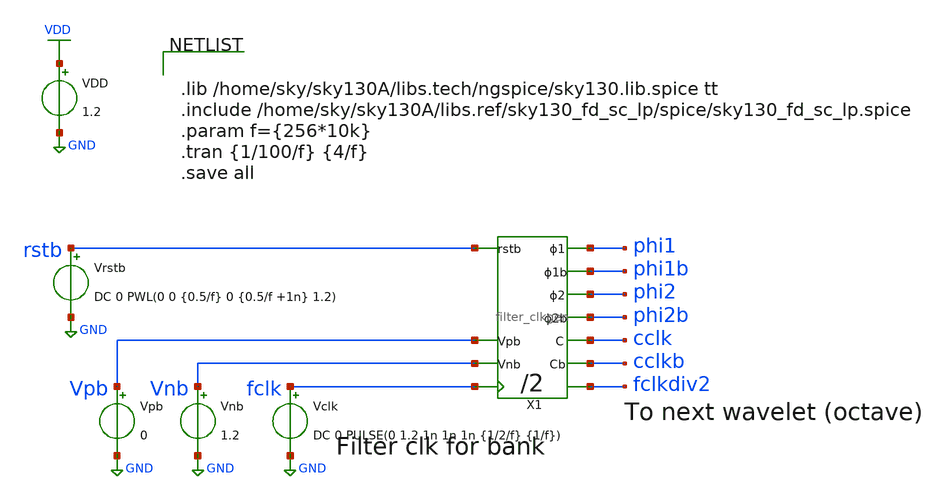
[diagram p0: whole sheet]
** sch_path: xschem/clkgen/filter_clkgen_tb.sch
**.subckt filter_clkgen_tb
Vrstb rstb GND DC 0 PWL(0 0 {0.5/f} 0 {0.5/f +1n} 1.2)
VDD VDD GND 1.2
Vpb Vpb GND 0
Vnb Vnb GND 1.2
Vclk fclk GND DC 0 PULSE(0 1.2 1n 1n 1n {1/2/f} {1/f})
X1 rstb fclk phi2b phi2 phi1b phi1 cclkb cclk fclkdiv2 Vpb Vnb filter_clkgen
**** begin user architecture code


.lib /home/sky/sky130A/libs.tech/ngspice/sky130.lib.spice tt
.include /home/sky/sky130A/libs.ref/sky130_fd_sc_lp/spice/sky130_fd_sc_lp.spice
.param f={256*10k}
.tran {1/100/f} {4/f}
.save all


**** end user architecture code
**.ends

* expanding   symbol:  clkgen/filter_clkgen.sym # of pins=11
** sym_path: xschem/clkgen/filter_clkgen.sym
** sch_path: xschem/clkgen/filter_clkgen.sch
.subckt filter_clkgen rstb clk phi2b phi2 phi1b phi1 cclkb cclk clkdiv2 Vpb Vnb
*.ipin clk
*.ipin rstb
*.opin phi2
*.opin phi2b
*.opin phi1
*.opin phi1b
*.opin cclk
*.opin cclkb
*.opin clkdiv2
*.ipin Vpb
*.ipin Vnb
x11 clk net3 rstb gnd gnd vdd vdd clkdiv2 net3 sky130_fd_sc_lp__dfrbp_1
X4 phi2dd phi2 phi2b comp_clks Wpmos=1.26 Lpmos=0.18 Wnmos=0.42 Lnmos=0.18
X7 phi1dd phi1 phi1b comp_clks Wpmos=1.26 Lpmos=0.18 Wnmos=0.42 Lnmos=0.18
X10 div2dd cclk cclkb comp_clks Wpmos=1.26 Lpmos=0.18 Wnmos=0.42 Lnmos=0.18
x12 clk rstb gnd gnd vdd vdd gclk sky130_fd_sc_lp__dlclkp_1
X1 gclk net1 net2 comp_clks_1stage Wpmos=1.26 Lpmos=0.18 Wnmos=0.42 Lnmos=0.18
x2 clk clkdiv2 gnd gnd vdd vdd net4 sky130_fd_sc_lp__and2_0
X2 net1 phi2d Vnb inv_weak_pulldown Wpmos=1.26 Lpmos= Wnmos= Lnmos=0.54
X5 net2 phi1d Vnb inv_weak_pulldown Wpmos=1.26 Lpmos= Wnmos= Lnmos=0.54
X8 net4 div2d Vnb inv_weak_pulldown Wpmos=1.26 Lpmos= Wnmos= Lnmos=0.54
X9 div2d div2dd Vnb inv_weak_pulldown Wpmos=1.26 Lpmos= Wnmos= Lnmos=0.54
X3 phi2d phi2dd Vpb inv_weak_pullup Wpmos=1.26 Lpmos=0.54 Wnmos= Lnmos=
X6 phi1d phi1dd Vpb inv_weak_pullup Wpmos=1.26 Lpmos=0.54 Wnmos= Lnmos=
.ends


* expanding   symbol:  clkgen/comp_clks.sym # of pins=3
** sym_path: xschem/clkgen/comp_clks.sym
** sch_path: xschem/clkgen/comp_clks.sch
.subckt comp_clks clk clka clkb  Wpmos=3 Lpmos=0.18 Wnmos=1 Lnmos=0.18
*.ipin clk
*.opin clka
*.opin clkb
X3 clk clkt GND VDD transmission_gate Wpmos=Wpmos Lpmos=Lpmos Wnmos=Wnmos Lnmos=Lnmos
X1 clk clki inv Wpmos=3 Lpmos=0.18 Wnmos=1 Lnmos=0.18
X2 clki clka inv Wpmos=3 Lpmos=0.18 Wnmos=1 Lnmos=0.18
X4 clkt clkb inv Wpmos=3 Lpmos=0.18 Wnmos=1 Lnmos=0.18
.ends


* expanding   symbol:  clkgen/comp_clks_1stage.sym # of pins=3
** sym_path: xschem/clkgen/comp_clks_1stage.sym
** sch_path: xschem/clkgen/comp_clks_1stage.sch
.subckt comp_clks_1stage clk clka clkb  Wpmos=1.26 Lpmos=0.18 Wnmos=0.42 Lnmos=0.18
*.ipin clk
*.opin clka
*.opin clkb
X3 clk clkb GND VDD transmission_gate Wpmos=Wpmos Lpmos=Lpmos Wnmos=Wnmos Lnmos=Lnmos
X1 clk clka inv Wpmos=Wpmos Lpmos=Lpmos Wnmos=Wnmos Lnmos=Lnmos
.ends


* expanding   symbol:  inv/inv_weak_pulldown.sym # of pins=3
** sym_path: xschem/inv/inv_weak_pulldown.sym
** sch_path: xschem/inv/inv_weak_pulldown.sch
.subckt inv_weak_pulldown in out Vnb  Wpmos=1.26 Lmin=0.18 Wmin=0.42 Lnmos=0.54
*.ipin in
*.iopin out
*.ipin Vnb
XM1 net1 in GND GND sky130_fd_pr__nfet_01v8 L=Lmin W=Wmin nf=1 ad='int((nf+1)/2) * W/nf * 0.29' as='int((nf+2)/2) * W/nf * 0.29'
+ pd='2*int((nf+1)/2) * (W/nf + 0.29)' ps='2*int((nf+2)/2) * (W/nf + 0.29)' nrd='0.29 / W' nrs='0.29 / W'
+ sa=0 sb=0 sd=0 mult=1 m=1
XM2 out in VDD VDD sky130_fd_pr__pfet_01v8 L=Lmin W=Wpmos nf=1 ad='int((nf+1)/2) * W/nf * 0.29' as='int((nf+2)/2) * W/nf * 0.29'
+ pd='2*int((nf+1)/2) * (W/nf + 0.29)' ps='2*int((nf+2)/2) * (W/nf + 0.29)' nrd='0.29 / W' nrs='0.29 / W'
+ sa=0 sb=0 sd=0 mult=1 m=1
XM3 out Vnb net1 GND sky130_fd_pr__nfet_01v8 L=Lnmos W=Wmin nf=1 ad='int((nf+1)/2) * W/nf * 0.29' as='int((nf+2)/2) * W/nf * 0.29'
+ pd='2*int((nf+1)/2) * (W/nf + 0.29)' ps='2*int((nf+2)/2) * (W/nf + 0.29)' nrd='0.29 / W' nrs='0.29 / W'
+ sa=0 sb=0 sd=0 mult=1 m=1
.ends


* expanding   symbol:  inv/inv_weak_pullup.sym # of pins=3
** sym_path: xschem/inv/inv_weak_pullup.sym
** sch_path: xschem/inv/inv_weak_pullup.sch
.subckt inv_weak_pullup in out Vpb  Wpmos=1.26 Lpmos=0.54 Wmin=0.42 Lmin=0.18
*.ipin in
*.iopin out
*.ipin Vpb
XM1 out in GND GND sky130_fd_pr__nfet_01v8 L=Lmin W=Wmin nf=1 ad='int((nf+1)/2) * W/nf * 0.29' as='int((nf+2)/2) * W/nf * 0.29'
+ pd='2*int((nf+1)/2) * (W/nf + 0.29)' ps='2*int((nf+2)/2) * (W/nf + 0.29)' nrd='0.29 / W' nrs='0.29 / W'
+ sa=0 sb=0 sd=0 mult=1 m=1
XM2 net1 in VDD VDD sky130_fd_pr__pfet_01v8 L=Lmin W=Wpmos nf=1 ad='int((nf+1)/2) * W/nf * 0.29' as='int((nf+2)/2) * W/nf * 0.29'
+ pd='2*int((nf+1)/2) * (W/nf + 0.29)' ps='2*int((nf+2)/2) * (W/nf + 0.29)' nrd='0.29 / W' nrs='0.29 / W'
+ sa=0 sb=0 sd=0 mult=1 m=1
XM3 out Vpb net1 VDD sky130_fd_pr__pfet_01v8 L=Lpmos W=Wpmos nf=1 ad='int((nf+1)/2) * W/nf * 0.29' as='int((nf+2)/2) * W/nf * 0.29'
+ pd='2*int((nf+1)/2) * (W/nf + 0.29)' ps='2*int((nf+2)/2) * (W/nf + 0.29)' nrd='0.29 / W' nrs='0.29 / W'
+ sa=0 sb=0 sd=0 mult=1 m=1
.ends


* expanding   symbol:  transmission_gate/transmission_gate.sym # of pins=4
** sym_path: xschem/transmission_gate/transmission_gate.sym
** sch_path: xschem/transmission_gate/transmission_gate.sch
.subckt transmission_gate in out ctrl_ ctrl  Wpmos=0.42 Lpmos=0.18 Wnmos=0.42 Lnmos=0.18
*.iopin in
*.iopin out
*.ipin ctrl_
*.ipin ctrl
XM1 out ctrl in GND sky130_fd_pr__nfet_01v8 L=Lnmos W=Wnmos nf=1 ad='int((nf+1)/2) * W/nf * 0.29' as='int((nf+2)/2) * W/nf * 0.29'
+ pd='2*int((nf+1)/2) * (W/nf + 0.29)' ps='2*int((nf+2)/2) * (W/nf + 0.29)' nrd='0.29 / W' nrs='0.29 / W'
+ sa=0 sb=0 sd=0 mult=1 m=1
XM2 out ctrl_ in VDD sky130_fd_pr__pfet_01v8 L=Lpmos W=Wpmos nf=1 ad='int((nf+1)/2) * W/nf * 0.29' as='int((nf+2)/2) * W/nf * 0.29'
+ pd='2*int((nf+1)/2) * (W/nf + 0.29)' ps='2*int((nf+2)/2) * (W/nf + 0.29)' nrd='0.29 / W' nrs='0.29 / W'
+ sa=0 sb=0 sd=0 mult=1 m=1
.ends


* expanding   symbol:  inv/inv.sym # of pins=2
** sym_path: xschem/inv/inv.sym
** sch_path: xschem/inv/inv.sch
.subckt inv in out  Wpmos=3 Lpmos=0.18 Wnmos=1 Lnmos=0.18
*.ipin in
*.iopin out
XM1 out in GND GND sky130_fd_pr__nfet_01v8 L=Lnmos W=Wnmos nf=1 ad='int((nf+1)/2) * W/nf * 0.29' as='int((nf+2)/2) * W/nf * 0.29'
+ pd='2*int((nf+1)/2) * (W/nf + 0.29)' ps='2*int((nf+2)/2) * (W/nf + 0.29)' nrd='0.29 / W' nrs='0.29 / W'
+ sa=0 sb=0 sd=0 mult=1 m=1
XM2 out in VDD VDD sky130_fd_pr__pfet_01v8 L=Lpmos W=Wpmos nf=1 ad='int((nf+1)/2) * W/nf * 0.29' as='int((nf+2)/2) * W/nf * 0.29'
+ pd='2*int((nf+1)/2) * (W/nf + 0.29)' ps='2*int((nf+2)/2) * (W/nf + 0.29)' nrd='0.29 / W' nrs='0.29 / W'
+ sa=0 sb=0 sd=0 mult=1 m=1
.ends

.GLOBAL VDD
.GLOBAL GND
.end
